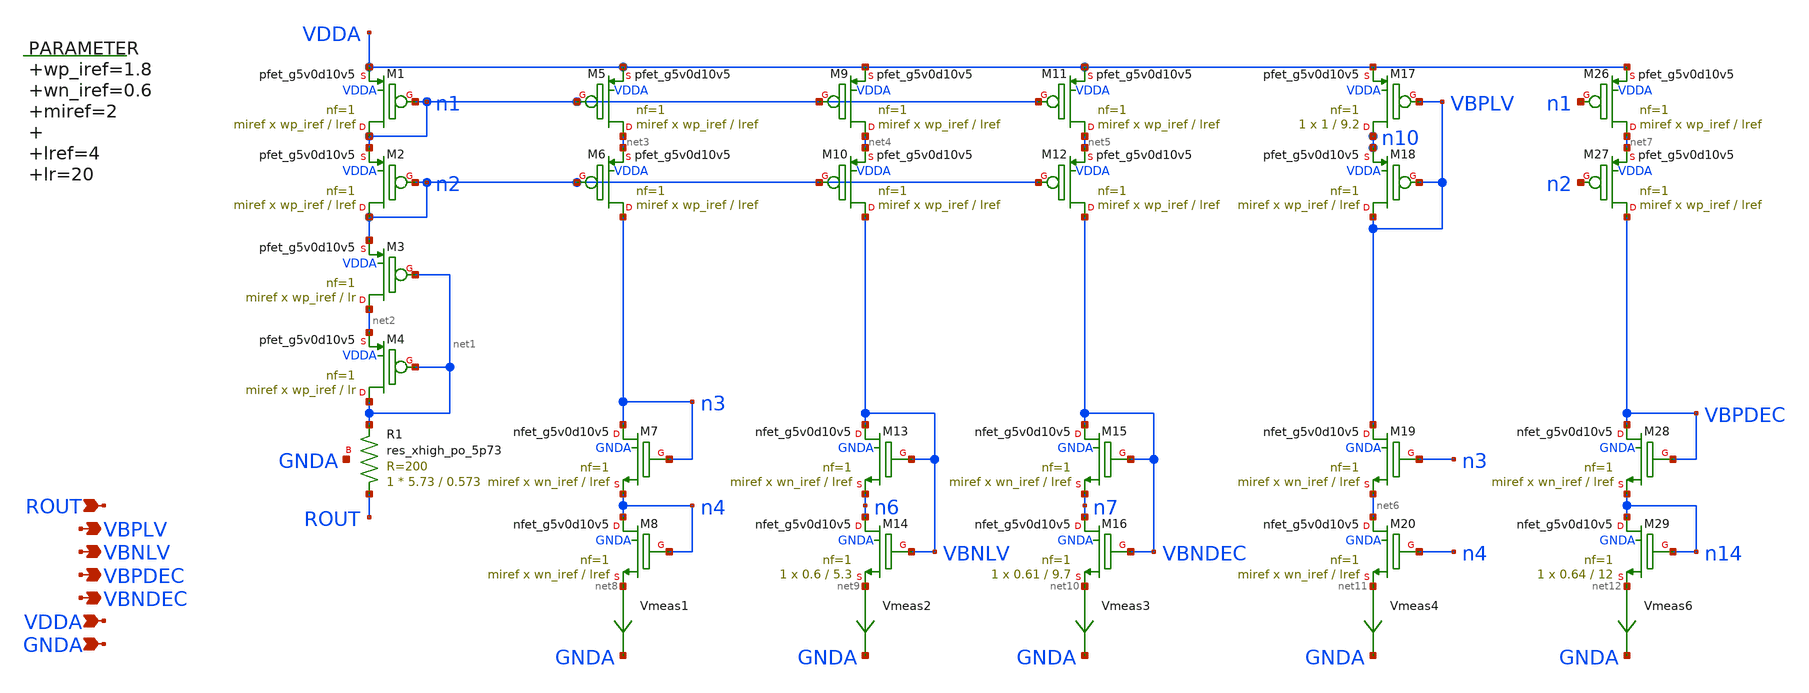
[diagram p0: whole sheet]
** sch_path: xschem/bias_lvsf.sch
**.subckt bias_lvsf ROUT VBPLV VBNLV VBPDEC VBNDEC VDDA GNDA
*.ipin ROUT
*.opin VBPLV
*.opin VBNLV
*.opin VBPDEC
*.opin VBNDEC
*.ipin VDDA
*.ipin GNDA
XM1 n1 n1 VDDA VDDA sky130_fd_pr__pfet_g5v0d10v5 L=lref W=wp_iref nf=1 ad='int((nf+1)/2) * W/nf * 0.29'
+ as='int((nf+2)/2) * W/nf * 0.29' pd='2*int((nf+1)/2) * (W/nf + 0.29)' ps='2*int((nf+2)/2) * (W/nf + 0.29)'
+ nrd='0.29 / W' nrs='0.29 / W' sa=0 sb=0 sd=0 mult=miref m=miref
.param wp_iref=1.8 wn_iref=0.6 miref=2 lref=4 lr=20
XM2 n2 n2 n1 VDDA sky130_fd_pr__pfet_g5v0d10v5 L=lref W=wp_iref nf=1 ad='int((nf+1)/2) * W/nf * 0.29'
+ as='int((nf+2)/2) * W/nf * 0.29' pd='2*int((nf+1)/2) * (W/nf + 0.29)' ps='2*int((nf+2)/2) * (W/nf + 0.29)'
+ nrd='0.29 / W' nrs='0.29 / W' sa=0 sb=0 sd=0 mult=miref m=miref
XR1 ROUT net1 GNDA sky130_fd_pr__res_xhigh_po_5p73 L=0.573 mult=1 m=1
XM3 net2 net1 n2 VDDA sky130_fd_pr__pfet_g5v0d10v5 L=lr W=wp_iref nf=1 ad='int((nf+1)/2) * W/nf * 0.29'
+ as='int((nf+2)/2) * W/nf * 0.29' pd='2*int((nf+1)/2) * (W/nf + 0.29)' ps='2*int((nf+2)/2) * (W/nf + 0.29)'
+ nrd='0.29 / W' nrs='0.29 / W' sa=0 sb=0 sd=0 mult=miref m=miref
XM4 net1 net1 net2 VDDA sky130_fd_pr__pfet_g5v0d10v5 L=lr W=wp_iref nf=1 ad='int((nf+1)/2) * W/nf * 0.29'
+ as='int((nf+2)/2) * W/nf * 0.29' pd='2*int((nf+1)/2) * (W/nf + 0.29)' ps='2*int((nf+2)/2) * (W/nf + 0.29)'
+ nrd='0.29 / W' nrs='0.29 / W' sa=0 sb=0 sd=0 mult=miref m=miref
XM5 net3 n1 VDDA VDDA sky130_fd_pr__pfet_g5v0d10v5 L=lref W=wp_iref nf=1 ad='int((nf+1)/2) * W/nf * 0.29'
+ as='int((nf+2)/2) * W/nf * 0.29' pd='2*int((nf+1)/2) * (W/nf + 0.29)' ps='2*int((nf+2)/2) * (W/nf + 0.29)'
+ nrd='0.29 / W' nrs='0.29 / W' sa=0 sb=0 sd=0 mult=miref m=miref
XM6 n3 n2 net3 VDDA sky130_fd_pr__pfet_g5v0d10v5 L=lref W=wp_iref nf=1 ad='int((nf+1)/2) * W/nf * 0.29'
+ as='int((nf+2)/2) * W/nf * 0.29' pd='2*int((nf+1)/2) * (W/nf + 0.29)' ps='2*int((nf+2)/2) * (W/nf + 0.29)'
+ nrd='0.29 / W' nrs='0.29 / W' sa=0 sb=0 sd=0 mult=miref m=miref
Vmeas1 net8 GNDA 0
.save i(vmeas1)
XM7 n3 n3 n4 GNDA sky130_fd_pr__nfet_g5v0d10v5 L=lref W=wn_iref nf=1 ad='int((nf+1)/2) * W/nf * 0.29'
+ as='int((nf+2)/2) * W/nf * 0.29' pd='2*int((nf+1)/2) * (W/nf + 0.29)' ps='2*int((nf+2)/2) * (W/nf + 0.29)'
+ nrd='0.29 / W' nrs='0.29 / W' sa=0 sb=0 sd=0 mult=miref m=miref
XM8 n4 n4 net8 GNDA sky130_fd_pr__nfet_g5v0d10v5 L=lref W=wn_iref nf=1 ad='int((nf+1)/2) * W/nf * 0.29'
+ as='int((nf+2)/2) * W/nf * 0.29' pd='2*int((nf+1)/2) * (W/nf + 0.29)' ps='2*int((nf+2)/2) * (W/nf + 0.29)'
+ nrd='0.29 / W' nrs='0.29 / W' sa=0 sb=0 sd=0 mult=miref m=miref
XM9 net4 n1 VDDA VDDA sky130_fd_pr__pfet_g5v0d10v5 L=lref W=wp_iref nf=1 ad='int((nf+1)/2) * W/nf * 0.29'
+ as='int((nf+2)/2) * W/nf * 0.29' pd='2*int((nf+1)/2) * (W/nf + 0.29)' ps='2*int((nf+2)/2) * (W/nf + 0.29)'
+ nrd='0.29 / W' nrs='0.29 / W' sa=0 sb=0 sd=0 mult=miref m=miref
XM10 VBNLV n2 net4 VDDA sky130_fd_pr__pfet_g5v0d10v5 L=lref W=wp_iref nf=1 ad='int((nf+1)/2) * W/nf * 0.29'
+ as='int((nf+2)/2) * W/nf * 0.29' pd='2*int((nf+1)/2) * (W/nf + 0.29)' ps='2*int((nf+2)/2) * (W/nf + 0.29)'
+ nrd='0.29 / W' nrs='0.29 / W' sa=0 sb=0 sd=0 mult=miref m=miref
XM11 net5 n1 VDDA VDDA sky130_fd_pr__pfet_g5v0d10v5 L=lref W=wp_iref nf=1 ad='int((nf+1)/2) * W/nf * 0.29'
+ as='int((nf+2)/2) * W/nf * 0.29' pd='2*int((nf+1)/2) * (W/nf + 0.29)' ps='2*int((nf+2)/2) * (W/nf + 0.29)'
+ nrd='0.29 / W' nrs='0.29 / W' sa=0 sb=0 sd=0 mult=miref m=miref
XM12 VBNDEC n2 net5 VDDA sky130_fd_pr__pfet_g5v0d10v5 L=lref W=wp_iref nf=1 ad='int((nf+1)/2) * W/nf * 0.29'
+ as='int((nf+2)/2) * W/nf * 0.29' pd='2*int((nf+1)/2) * (W/nf + 0.29)' ps='2*int((nf+2)/2) * (W/nf + 0.29)'
+ nrd='0.29 / W' nrs='0.29 / W' sa=0 sb=0 sd=0 mult=miref m=miref
XM13 VBNLV VBNLV n6 GNDA sky130_fd_pr__nfet_g5v0d10v5 L=lref W=wn_iref nf=1 ad='int((nf+1)/2) * W/nf * 0.29'
+ as='int((nf+2)/2) * W/nf * 0.29' pd='2*int((nf+1)/2) * (W/nf + 0.29)' ps='2*int((nf+2)/2) * (W/nf + 0.29)'
+ nrd='0.29 / W' nrs='0.29 / W' sa=0 sb=0 sd=0 mult=miref m=miref
XM14 n6 VBNLV net9 GNDA sky130_fd_pr__nfet_g5v0d10v5 L=5.3 W=0.6 nf=1 ad='int((nf+1)/2) * W/nf * 0.29'
+ as='int((nf+2)/2) * W/nf * 0.29' pd='2*int((nf+1)/2) * (W/nf + 0.29)' ps='2*int((nf+2)/2) * (W/nf + 0.29)'
+ nrd='0.29 / W' nrs='0.29 / W' sa=0 sb=0 sd=0 mult=1 m=1
Vmeas2 net9 GNDA 0
.save i(vmeas2)
XM15 VBNDEC VBNDEC n7 GNDA sky130_fd_pr__nfet_g5v0d10v5 L=lref W=wn_iref nf=1 ad='int((nf+1)/2) * W/nf * 0.29'
+ as='int((nf+2)/2) * W/nf * 0.29' pd='2*int((nf+1)/2) * (W/nf + 0.29)' ps='2*int((nf+2)/2) * (W/nf + 0.29)'
+ nrd='0.29 / W' nrs='0.29 / W' sa=0 sb=0 sd=0 mult=miref m=miref
XM16 n7 VBNDEC net10 GNDA sky130_fd_pr__nfet_g5v0d10v5 L=9.7 W=0.61 nf=1 ad='int((nf+1)/2) * W/nf * 0.29'
+ as='int((nf+2)/2) * W/nf * 0.29' pd='2*int((nf+1)/2) * (W/nf + 0.29)' ps='2*int((nf+2)/2) * (W/nf + 0.29)'
+ nrd='0.29 / W' nrs='0.29 / W' sa=0 sb=0 sd=0 mult=1 m=1
Vmeas3 net10 GNDA 0
.save i(vmeas3)
XM17 n10 VBPLV VDDA VDDA sky130_fd_pr__pfet_g5v0d10v5 L=9.2 W=1 nf=1 ad='int((nf+1)/2) * W/nf * 0.29'
+ as='int((nf+2)/2) * W/nf * 0.29' pd='2*int((nf+1)/2) * (W/nf + 0.29)' ps='2*int((nf+2)/2) * (W/nf + 0.29)'
+ nrd='0.29 / W' nrs='0.29 / W' sa=0 sb=0 sd=0 mult=1 m=1
XM18 VBPLV VBPLV n10 VDDA sky130_fd_pr__pfet_g5v0d10v5 L=lref W=wp_iref nf=1 ad='int((nf+1)/2) * W/nf * 0.29'
+ as='int((nf+2)/2) * W/nf * 0.29' pd='2*int((nf+1)/2) * (W/nf + 0.29)' ps='2*int((nf+2)/2) * (W/nf + 0.29)'
+ nrd='0.29 / W' nrs='0.29 / W' sa=0 sb=0 sd=0 mult=miref m=miref
Vmeas4 net11 GNDA 0
.save i(vmeas4)
XM19 VBPLV n3 net6 GNDA sky130_fd_pr__nfet_g5v0d10v5 L=lref W=wn_iref nf=1 ad='int((nf+1)/2) * W/nf * 0.29'
+ as='int((nf+2)/2) * W/nf * 0.29' pd='2*int((nf+1)/2) * (W/nf + 0.29)' ps='2*int((nf+2)/2) * (W/nf + 0.29)'
+ nrd='0.29 / W' nrs='0.29 / W' sa=0 sb=0 sd=0 mult=miref m=miref
XM20 net6 n4 net11 GNDA sky130_fd_pr__nfet_g5v0d10v5 L=lref W=wn_iref nf=1 ad='int((nf+1)/2) * W/nf * 0.29'
+ as='int((nf+2)/2) * W/nf * 0.29' pd='2*int((nf+1)/2) * (W/nf + 0.29)' ps='2*int((nf+2)/2) * (W/nf + 0.29)'
+ nrd='0.29 / W' nrs='0.29 / W' sa=0 sb=0 sd=0 mult=miref m=miref
XM26 net7 n1 VDDA VDDA sky130_fd_pr__pfet_g5v0d10v5 L=lref W=wp_iref nf=1 ad='int((nf+1)/2) * W/nf * 0.29'
+ as='int((nf+2)/2) * W/nf * 0.29' pd='2*int((nf+1)/2) * (W/nf + 0.29)' ps='2*int((nf+2)/2) * (W/nf + 0.29)'
+ nrd='0.29 / W' nrs='0.29 / W' sa=0 sb=0 sd=0 mult=miref m=miref
XM27 VBPDEC n2 net7 VDDA sky130_fd_pr__pfet_g5v0d10v5 L=lref W=wp_iref nf=1 ad='int((nf+1)/2) * W/nf * 0.29'
+ as='int((nf+2)/2) * W/nf * 0.29' pd='2*int((nf+1)/2) * (W/nf + 0.29)' ps='2*int((nf+2)/2) * (W/nf + 0.29)'
+ nrd='0.29 / W' nrs='0.29 / W' sa=0 sb=0 sd=0 mult=miref m=miref
XM28 VBPDEC VBPDEC n14 GNDA sky130_fd_pr__nfet_g5v0d10v5 L=lref W=wn_iref nf=1 ad='int((nf+1)/2) * W/nf * 0.29'
+ as='int((nf+2)/2) * W/nf * 0.29' pd='2*int((nf+1)/2) * (W/nf + 0.29)' ps='2*int((nf+2)/2) * (W/nf + 0.29)'
+ nrd='0.29 / W' nrs='0.29 / W' sa=0 sb=0 sd=0 mult=miref m=miref
XM29 n14 n14 net12 GNDA sky130_fd_pr__nfet_g5v0d10v5 L=12 W=0.64 nf=1 ad='int((nf+1)/2) * W/nf * 0.29'
+ as='int((nf+2)/2) * W/nf * 0.29' pd='2*int((nf+1)/2) * (W/nf + 0.29)' ps='2*int((nf+2)/2) * (W/nf + 0.29)'
+ nrd='0.29 / W' nrs='0.29 / W' sa=0 sb=0 sd=0 mult=1 m=1
Vmeas6 net12 GNDA 0
.save i(vmeas6)
**.ends
.end
